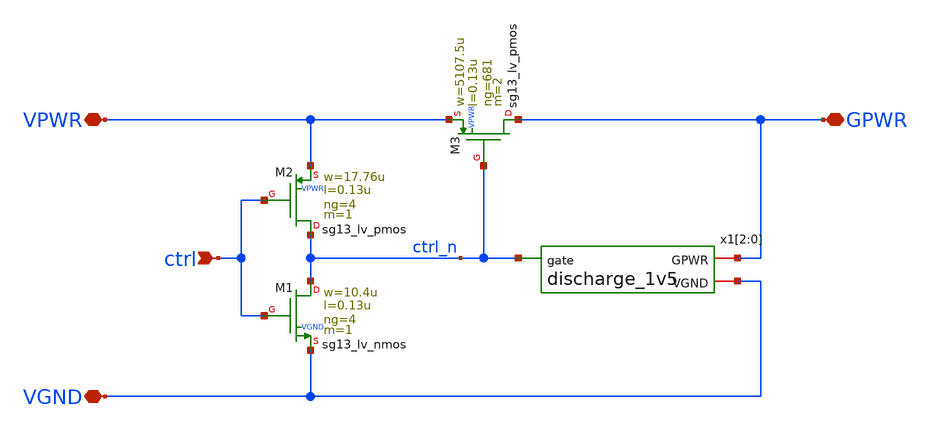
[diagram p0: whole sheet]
** sch_path: pg/ihp-sg13cmos5l/tt_pg_1v5_hp_4/xschem/tt_pg_1v5_hp_4.sch
**.subckt tt_pg_1v5_hp_4 ctrl VPWR VGND GPWR
*.ipin ctrl
*.iopin VPWR
*.iopin VGND
*.iopin GPWR
XM1 ctrl_n ctrl VGND VGND sg13_lv_nmos w=10.4u l=0.13u ng=4 m=1
XM2 ctrl_n ctrl VPWR VPWR sg13_lv_pmos w=17.76u l=0.13u ng=4 m=1
XM3 GPWR ctrl_n VPWR VPWR sg13_lv_pmos w=5107.5u l=0.13u ng=681 m=2
x1[2] VGND GPWR ctrl_n discharge_1v5
x1[1] VGND GPWR ctrl_n discharge_1v5
x1[0] VGND GPWR ctrl_n discharge_1v5
**.ends

* expanding   symbol:  discharge_1v5.sym # of pins=3
** sym_path: pg/ihp-sg13cmos5l/common/xschem/discharge_1v5.sym
** sch_path: pg/ihp-sg13cmos5l/common/xschem/discharge_1v5.sch
.subckt discharge_1v5 VGND GPWR gate
*.iopin GPWR
*.iopin VGND
*.ipin gate
XM1 GPWR gate net3 VGND sg13_lv_nmos w=0.50u l=0.65u ng=1 m=1
XM2 net3 gate net2 VGND sg13_lv_nmos w=0.50u l=0.65u ng=1 m=1
XM3 net2 gate net1 VGND sg13_lv_nmos w=0.50u l=0.65u ng=1 m=1
XM4 net1 gate VGND VGND sg13_lv_nmos w=0.50u l=0.65u ng=1 m=1
XM5 GPWR gate net6 VGND sg13_lv_nmos w=0.50u l=0.65u ng=1 m=1
XM6 net6 gate net5 VGND sg13_lv_nmos w=0.50u l=0.65u ng=1 m=1
XM7 net5 gate net4 VGND sg13_lv_nmos w=0.50u l=0.65u ng=1 m=1
XM8 net4 gate VGND VGND sg13_lv_nmos w=0.50u l=0.65u ng=1 m=1
.ends

.end
